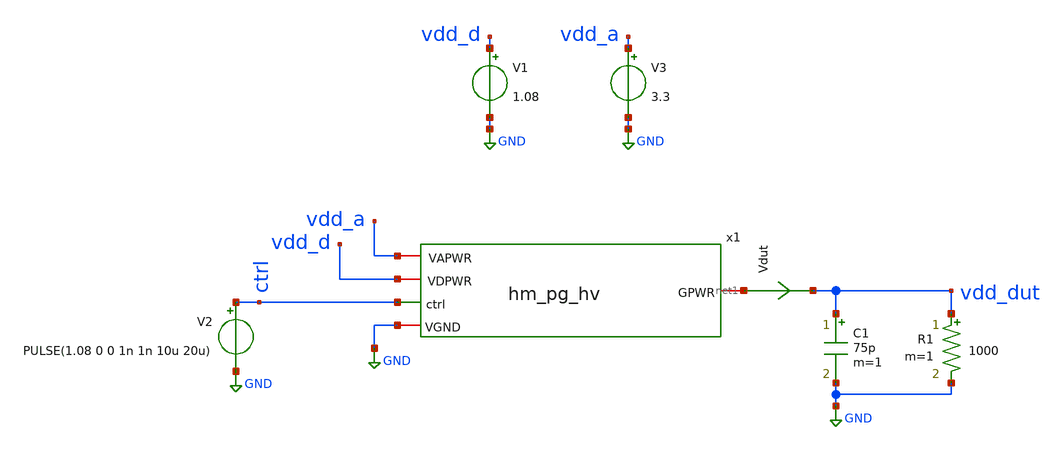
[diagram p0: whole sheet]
** sch_path: ihp-sg13cmos5l/libs.tech/xschem/tests/tb_hm_pg_hv_onoff.sch
**.subckt tb_hm_pg_hv_onoff
V1 vdd_d GND 1.08
.save i(v1)
C1 vdd_dut GND 75p m=1
Vdut net1 vdd_dut 0
.save i(vdut)
R1 vdd_dut GND 1000 m=1
V3 vdd_a GND 3.3
.save i(v3)
x1 net1 vdd_a vdd_d ctrl GND hm_pg_hv
V2 ctrl GND PULSE(1.08 0 0 1n 1n 10u 20u)
**** begin user architecture code

.lib cornerMOShv.lib mos_sf
.lib cornerMOSlv.lib mos_sf
*.lib cornerCAP.lib cap_typ




.control
save all

tran 10n 50u

plot vdd_dut
plot ctrl x1.h_crtl_p
plot ctrl x1.x2.ccp x1.x2.ccn

.endc


**** end user architecture code
**.ends

* expanding   symbol:
*+  /foss/designs/hm-openpdk-library/ihp-sg13cmos5l/libs.tech/xschem/hm_analog/hm_pg_hv.sym # of pins=5
** sym_path: ihp-sg13cmos5l/libs.tech/xschem/hm_analog/hm_pg_hv.sym
** sch_path: ihp-sg13cmos5l/libs.tech/xschem/hm_analog/hm_pg_hv.sch
.subckt hm_pg_hv GPWR VAPWR VDPWR ctrl VGND
*.ipin ctrl
*.iopin VAPWR
*.iopin VGND
*.iopin GPWR
*.iopin VDPWR
x2 VAPWR VDPWR ctrl H_crtl_p H_crtl_n VGND lv2hv
XM4 ctrl_n H_crtl_p VGND VGND sg13_hv_nmos w=2.6u l=0.45u ng=1 m=1 mm_ok=1
XM5 ctrl_n H_crtl_p VAPWR VAPWR sg13_hv_pmos w=4.44u l=0.45u ng=1 m=1 mm_ok=1
XM1 GPWR ctrl_n VAPWR VAPWR sg13_hv_pmos w=1445.4u l=0.45u ng=219 m=2 mm_ok=1
x3 VGND GPWR ctrl_n hv_dischg
.ends


* expanding   symbol:
*+  /foss/designs/hm-openpdk-library/ihp-sg13cmos5l/libs.tech/xschem/hm_analog/lv2hv.sym # of pins=6
** sym_path: ihp-sg13cmos5l/libs.tech/xschem/hm_analog/lv2hv.sym
** sch_path: ihp-sg13cmos5l/libs.tech/xschem/hm_analog/lv2hv.sch
.subckt lv2hv VAPWR VDPWR in out_p out_n VGND
*.iopin VAPWR
*.iopin VGND
*.ipin in
*.iopin VDPWR
*.opin out_p
*.opin out_n
XM1 in_n in VGND VGND sg13_lv_nmos w=1u l=0.13u ng=1 m=1 mm_ok=1
XM2 in_n in VDPWR VDPWR sg13_lv_pmos w=2u l=0.13u ng=1 m=1 mm_ok=1
XM3 in_p in_n VGND VGND sg13_lv_nmos w=1u l=0.13u ng=1 m=1 mm_ok=1
XM4 in_p in_n VDPWR VDPWR sg13_lv_pmos w=2u l=0.13u ng=1 m=1 mm_ok=1
XM5 out_p ccp VGND VGND sg13_hv_nmos w=1u l=0.45u ng=1 m=1 mm_ok=1
XM6 ccp in_p VGND VGND sg13_hv_nmos w=4u l=0.45u ng=1 m=1 mm_ok=1
XM7 out_p ccp VAPWR VAPWR sg13_hv_pmos w=2u l=0.45u ng=1 m=1 mm_ok=1
XM8 ccp ccn VAPWR VAPWR sg13_hv_pmos w=1u l=0.4u ng=1 m=1 mm_ok=1
XM9 ccn ccp VAPWR VAPWR sg13_hv_pmos w=1u l=0.4u ng=1 m=1 mm_ok=1
XM10 ccn in_n VGND VGND sg13_hv_nmos w=4u l=0.45u ng=1 m=1 mm_ok=1
XM11 out_n ccn VGND VGND sg13_hv_nmos w=1u l=0.45u ng=1 m=1 mm_ok=1
XM12 out_n ccn VAPWR VAPWR sg13_hv_pmos w=2u l=0.45u ng=1 m=1 mm_ok=1
.ends


* expanding   symbol:
*+  /foss/designs/hm-openpdk-library/ihp-sg13cmos5l/libs.tech/xschem/hm_analog/hv_dischg.sym # of pins=3
** sym_path: ihp-sg13cmos5l/libs.tech/xschem/hm_analog/hv_dischg.sym
** sch_path: ihp-sg13cmos5l/libs.tech/xschem/hm_analog/hv_dischg.sch
.subckt hv_dischg VGND GPWR gate
*.iopin GPWR
*.iopin VGND
*.ipin gate
XM6 GPWR gate net6 VGND sg13_hv_nmos w=0.5u l=0.65u ng=1 m=1 mm_ok=1
XM7 net6 gate net5 VGND sg13_hv_nmos w=0.5u l=0.65u ng=1 m=1 mm_ok=1
XM8 net5 gate net4 VGND sg13_hv_nmos w=0.5u l=0.65u ng=1 m=1 mm_ok=1
XM9 net4 gate VGND VGND sg13_hv_nmos w=0.5u l=0.65u ng=1 m=1 mm_ok=1
XM1 GPWR gate net1 VGND sg13_hv_nmos w=0.5u l=0.65u ng=1 m=1 mm_ok=1
XM2 net1 gate net2 VGND sg13_hv_nmos w=0.5u l=0.65u ng=1 m=1 mm_ok=1
XM3 net2 gate net3 VGND sg13_hv_nmos w=0.5u l=0.65u ng=1 m=1 mm_ok=1
XM4 net3 gate VGND VGND sg13_hv_nmos w=0.5u l=0.65u ng=1 m=1 mm_ok=1
.ends

.GLOBAL GND
.end
